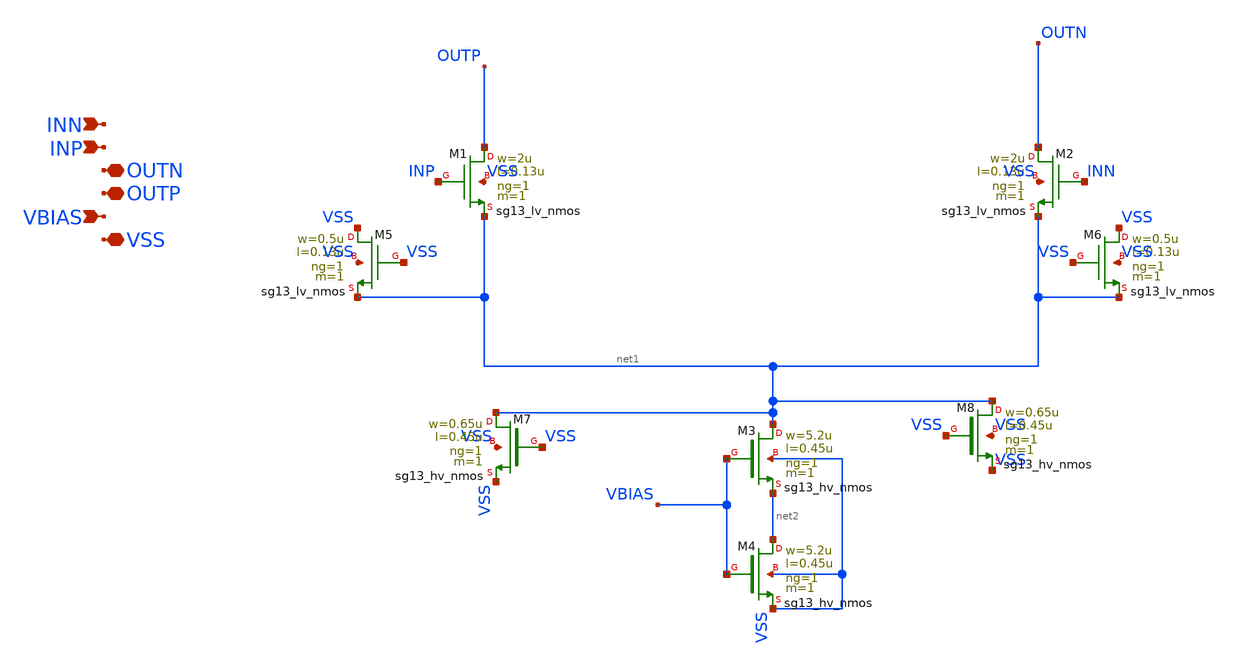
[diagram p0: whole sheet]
** sch_path: dependencies/DAC/DAC-main/schematic/xschem/CS_Switch_16x.sch
**.subckt CS_Switch_16x VSS VBIAS OUTP OUTN INP INN
*.iopin VSS
*.ipin VBIAS
*.iopin OUTP
*.iopin OUTN
*.ipin INP
*.ipin INN
XM1 OUTP INP net1 VSS sg13_lv_nmos w=2u l=0.13u ng=1 m=1 mm_ok=1
XM2 OUTN INN net1 VSS sg13_lv_nmos w=2u l=0.13u ng=1 m=1 mm_ok=1
XM3 net1 VBIAS net2 VSS sg13_hv_nmos w=5.2u l=0.45u ng=1 m=1 mm_ok=1
XM4 net2 VBIAS VSS VSS sg13_hv_nmos w=5.2u l=0.45u ng=1 m=1 mm_ok=1
XM5 VSS VSS net1 VSS sg13_lv_nmos w=0.5u l=0.13u ng=1 m=1 mm_ok=1
XM6 VSS VSS net1 VSS sg13_lv_nmos w=0.5u l=0.13u ng=1 m=1 mm_ok=1
XM7 net1 VSS VSS VSS sg13_hv_nmos w=0.65u l=0.45u ng=1 m=1 mm_ok=1
XM8 net1 VSS VSS VSS sg13_hv_nmos w=0.65u l=0.45u ng=1 m=1 mm_ok=1
**.ends
.end
